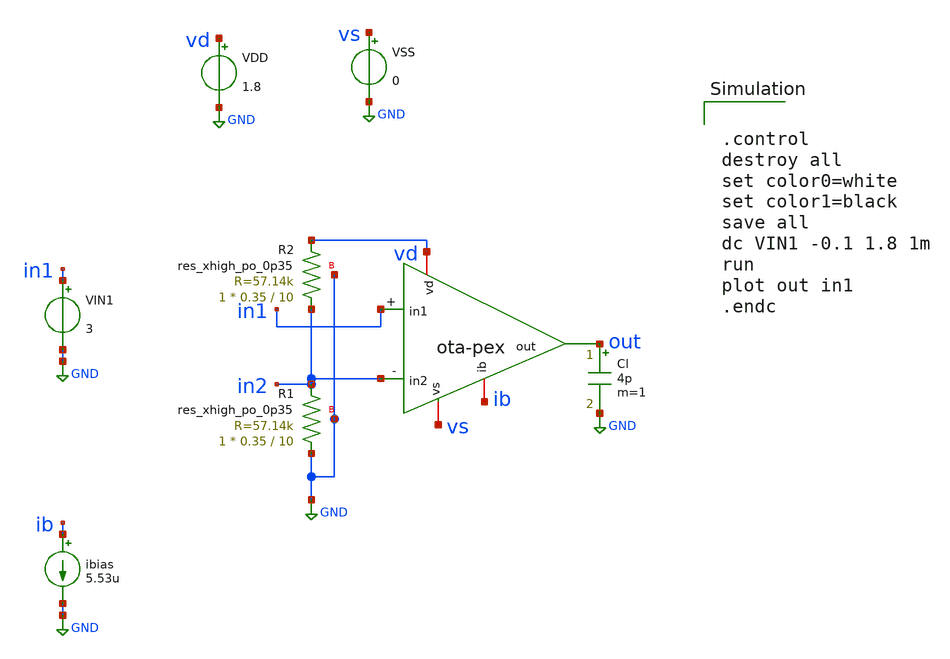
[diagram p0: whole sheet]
** sch_path: ota/xschem/ota_tb-dc.sch
* Copyright 2020 Stefan Frederik Schippers
* Licensed under the Apache License, Version 2.0 (the "License");
* you may not use this file except in compliance with the License.
* You may obtain a copy of the License at
* https://www.apache.org/licenses/LICENSE-2.0
* Unless required by applicable law or agreed to in writing, software
* distributed under the License is distributed on an "AS IS" BASIS,
* WITHOUT WARRANTIES OR CONDITIONS OF ANY KIND, either express or implied.
* See the License for the specific language governing permissions and
* limitations under the License.
**.subckt ota_tb-dc
VIN1 in1 GND 3
ibias ib GND 5.53u
VDD vd GND 1.8
VSS vs GND 0
Cl out GND 4p m=1
XR1 GND in2 GND sky130_fd_pr__res_xhigh_po_0p35 L=10 mult=1 m=1
XR2 in2 vd GND sky130_fd_pr__res_xhigh_po_0p35 L=10 mult=1 m=1
X1 vd ib out in2 in1 vs ota-pex
**** begin user architecture code


.control
destroy all
set color0=white
set color1=black
save all
dc VIN1 -0.1 1.8 1m
run
plot out in1
.endc

 .lib $::SKYWATER_MODELS/sky130.lib.spice tt
.include $::SKYWATER_STDCELLS/sky130_fd_sc_hd.spice

**** end user architecture code
**.ends
.GLOBAL GND
.end
